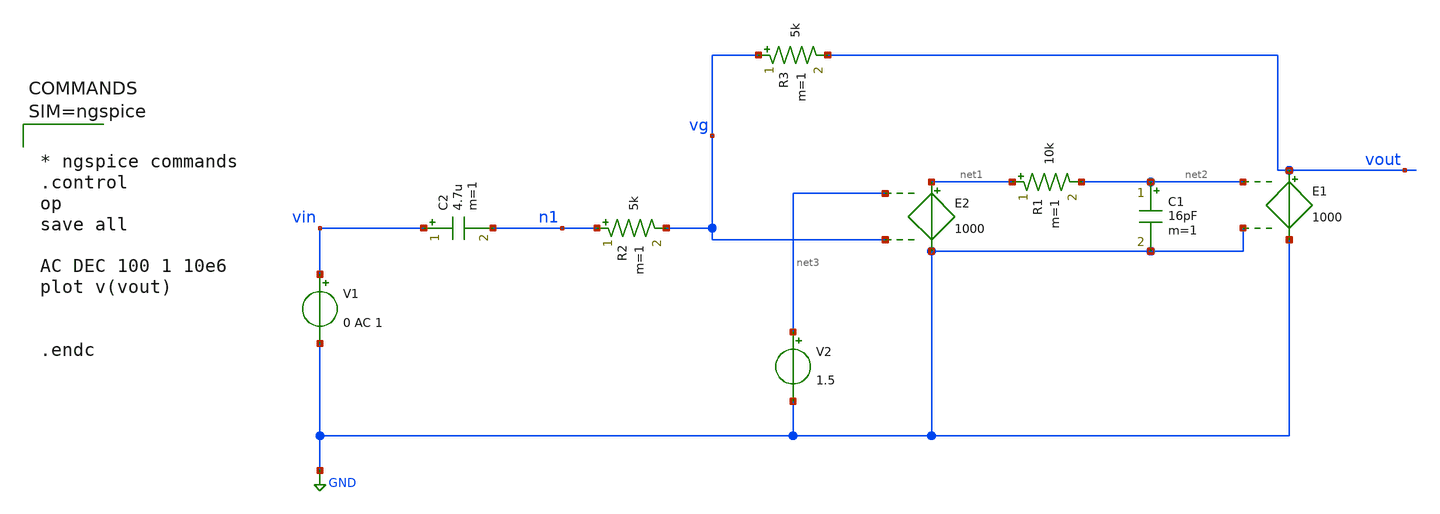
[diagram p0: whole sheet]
** sch_path: xschem/highpass_cascade.sch
**.subckt highpass_cascade
E1 vout GND net2 GND 1000
E2 net1 GND net3 vg 1000
C1 net2 GND 16pF m=1
R1 net1 net2 10k m=1
V1 vin GND 0 AC 1
C2 vin n1 4.7u m=1
R2 n1 vg 5k m=1
R3 vg vout 5k m=1
V2 net3 GND 1.5
**** begin user architecture code



* ngspice commands
.control
op
save all

AC DEC 100 1 10e6
plot v(vout)


.endc



**** end user architecture code
**.ends
.GLOBAL GND
.end
